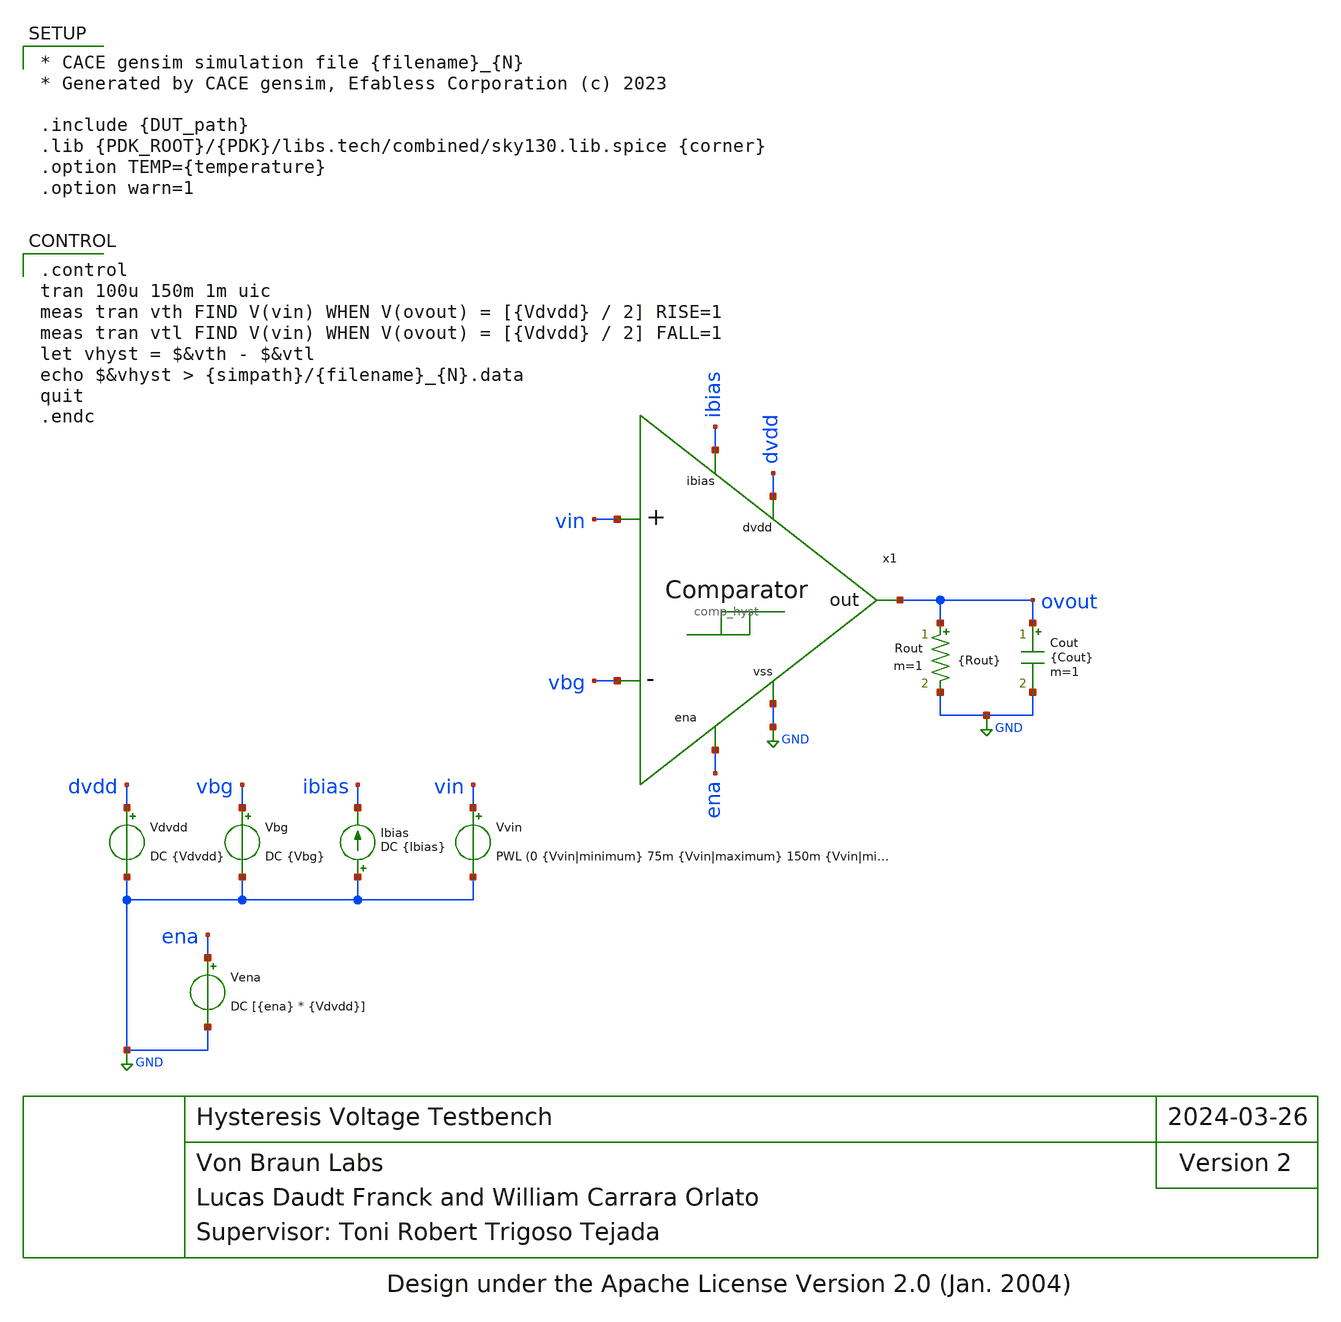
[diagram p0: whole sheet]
** sch_path: blocks/comp_hyst/cace/tb_vhyst.sch
* Design under the Apache License Version 2.0 (Jan. 2004)
**.subckt tb_vhyst
Vvin vin GND PWL (0 {Vvin|minimum} 75m {Vvin|maximum} 150m {Vvin|minimum})
Vdvdd dvdd GND DC {Vdvdd}
Vbg vbg GND DC {Vbg}
Ibias GND ibias DC {Ibias}
Vena ena GND DC [{ena} * {Vdvdd}]
Cout ovout GND {Cout} m=1
Rout ovout GND {Rout} m=1
x1 dvdd ovout vbg vin ena ibias GND comp_hyst
**** begin user architecture code

* CACE gensim simulation file {filename}_{N}
* Generated by CACE gensim, Efabless Corporation (c) 2023

.include {DUT_path}
.lib {PDK_ROOT}/{PDK}/libs.tech/combined/sky130.lib.spice {corner}
.option TEMP={temperature}
.option warn=1



.control
tran 100u 150m 1m uic
meas tran vth FIND V(vin) WHEN V(ovout) = [{Vdvdd} / 2] RISE=1
meas tran vtl FIND V(vin) WHEN V(ovout) = [{Vdvdd} / 2] FALL=1
let vhyst = $&vth - $&vtl
echo $&vhyst > {simpath}/{filename}_{N}.data
quit
.endc


**** end user architecture code
**.ends
.GLOBAL GND
.end
